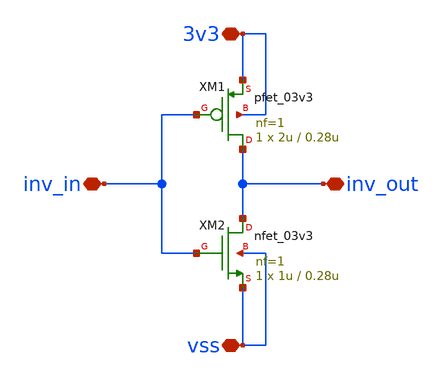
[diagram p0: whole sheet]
** sch_path: PLL/analog/schematics/Freq_Buffer_Inverter_DAC_Ref.sch
**.subckt Freq_Buffer_Inverter_DAC_Ref inv_in inv_out 3v3 vss
*.iopin inv_in
*.iopin inv_out
*.iopin 3v3
*.iopin vss
XM1 inv_out inv_in 3v3 3v3 pfet_03v3 L=0.28u W=2u nf=1 ad='int((nf+1)/2) * W/nf * 0.18u' as='int((nf+2)/2) * W/nf * 0.18u'
+ pd='2*int((nf+1)/2) * (W/nf + 0.18u)' ps='2*int((nf+2)/2) * (W/nf + 0.18u)' nrd='0.18u / W' nrs='0.18u / W'
+ sa=0 sb=0 sd=0 m=1
XM2 inv_out inv_in vss vss nfet_03v3 L=0.28u W=1u nf=1 ad='int((nf+1)/2) * W/nf * 0.18u' as='int((nf+2)/2) * W/nf * 0.18u'
+ pd='2*int((nf+1)/2) * (W/nf + 0.18u)' ps='2*int((nf+2)/2) * (W/nf + 0.18u)' nrd='0.18u / W' nrs='0.18u / W'
+ sa=0 sb=0 sd=0 m=1
**.ends
.end
